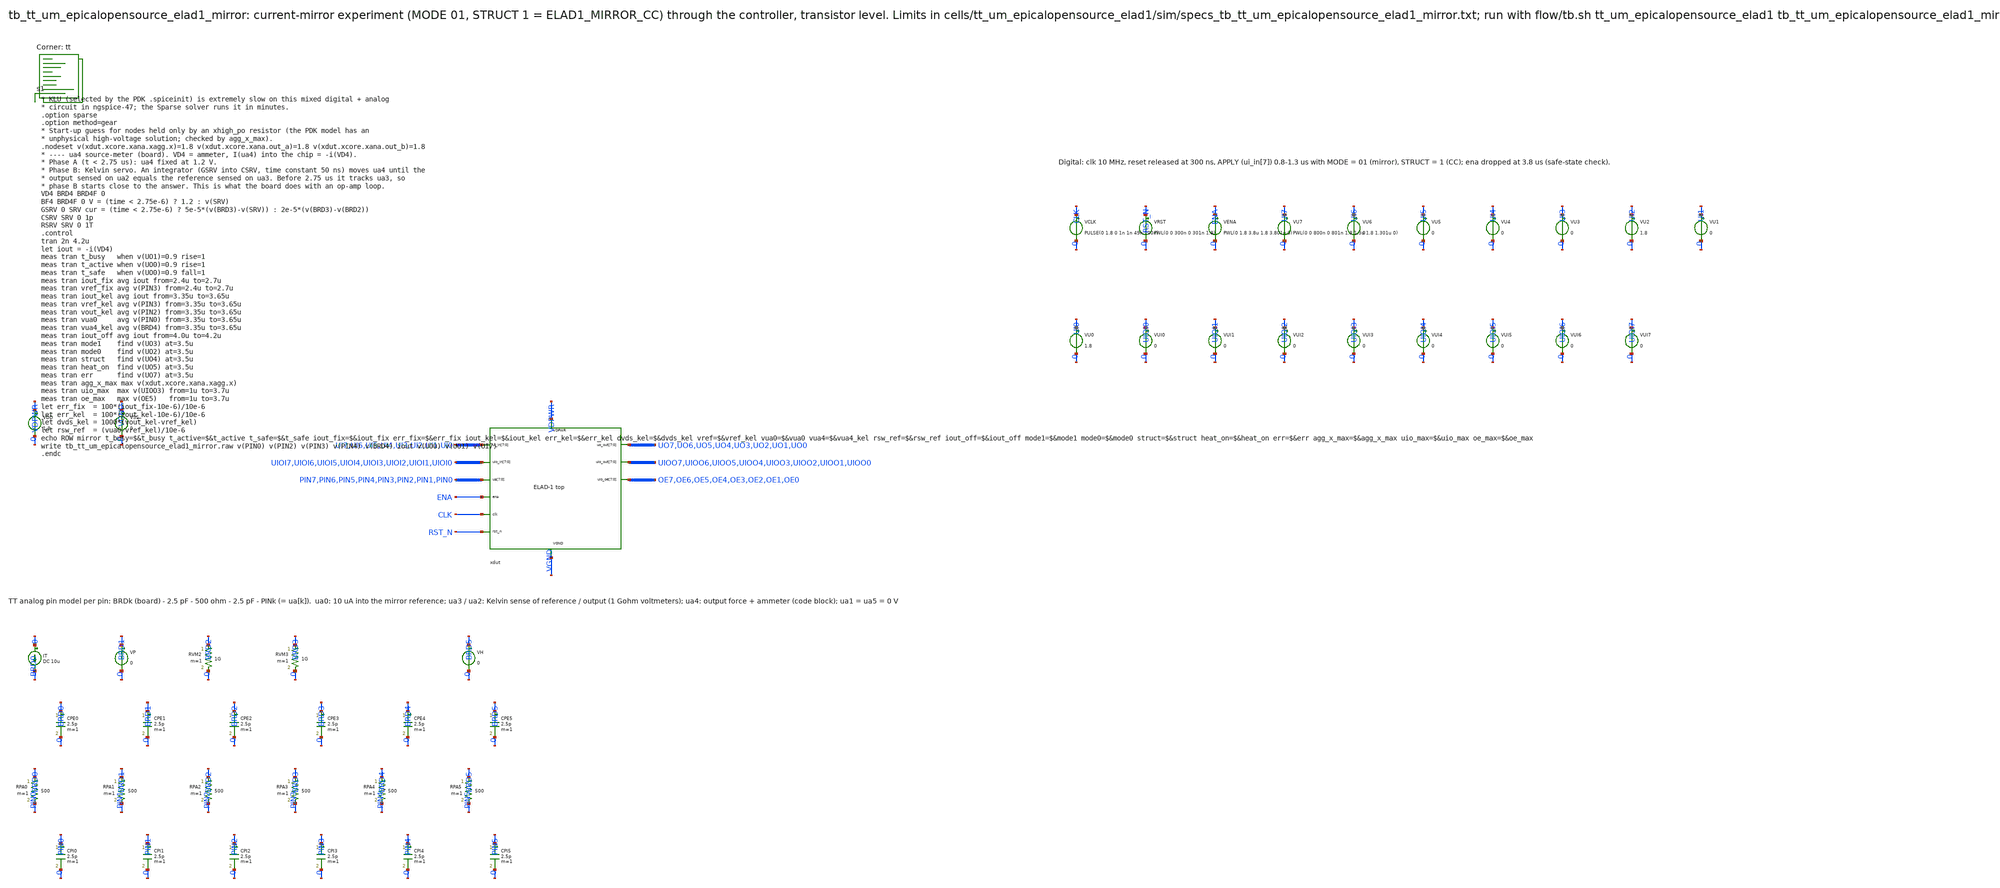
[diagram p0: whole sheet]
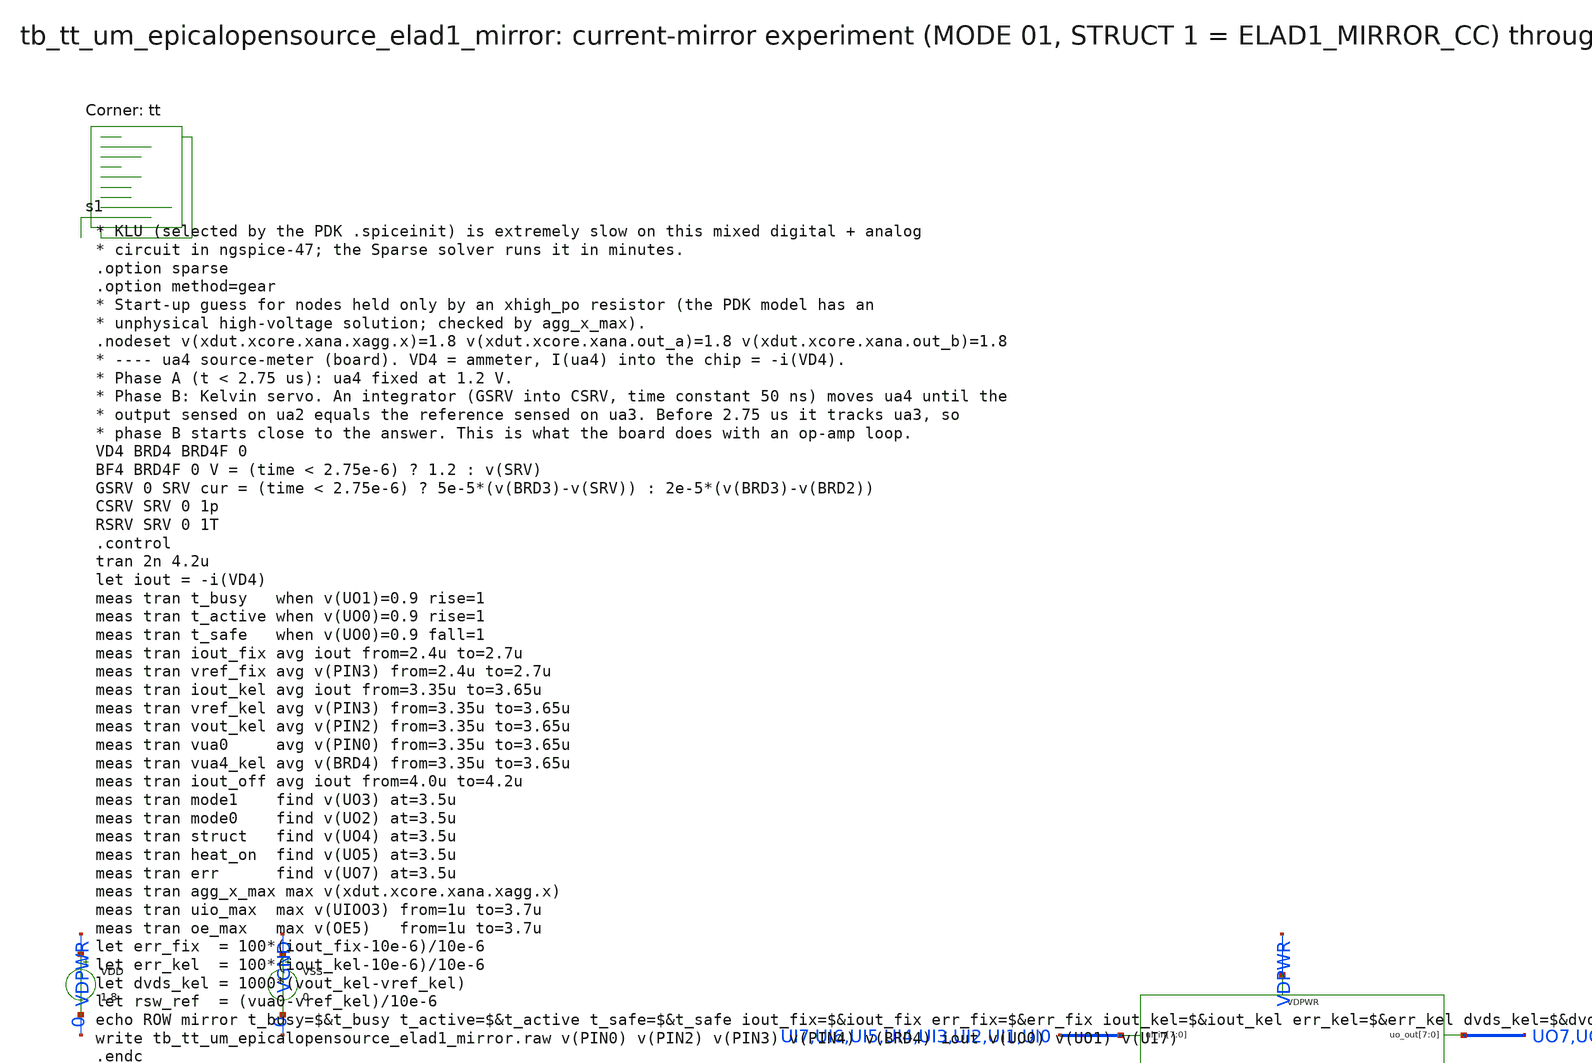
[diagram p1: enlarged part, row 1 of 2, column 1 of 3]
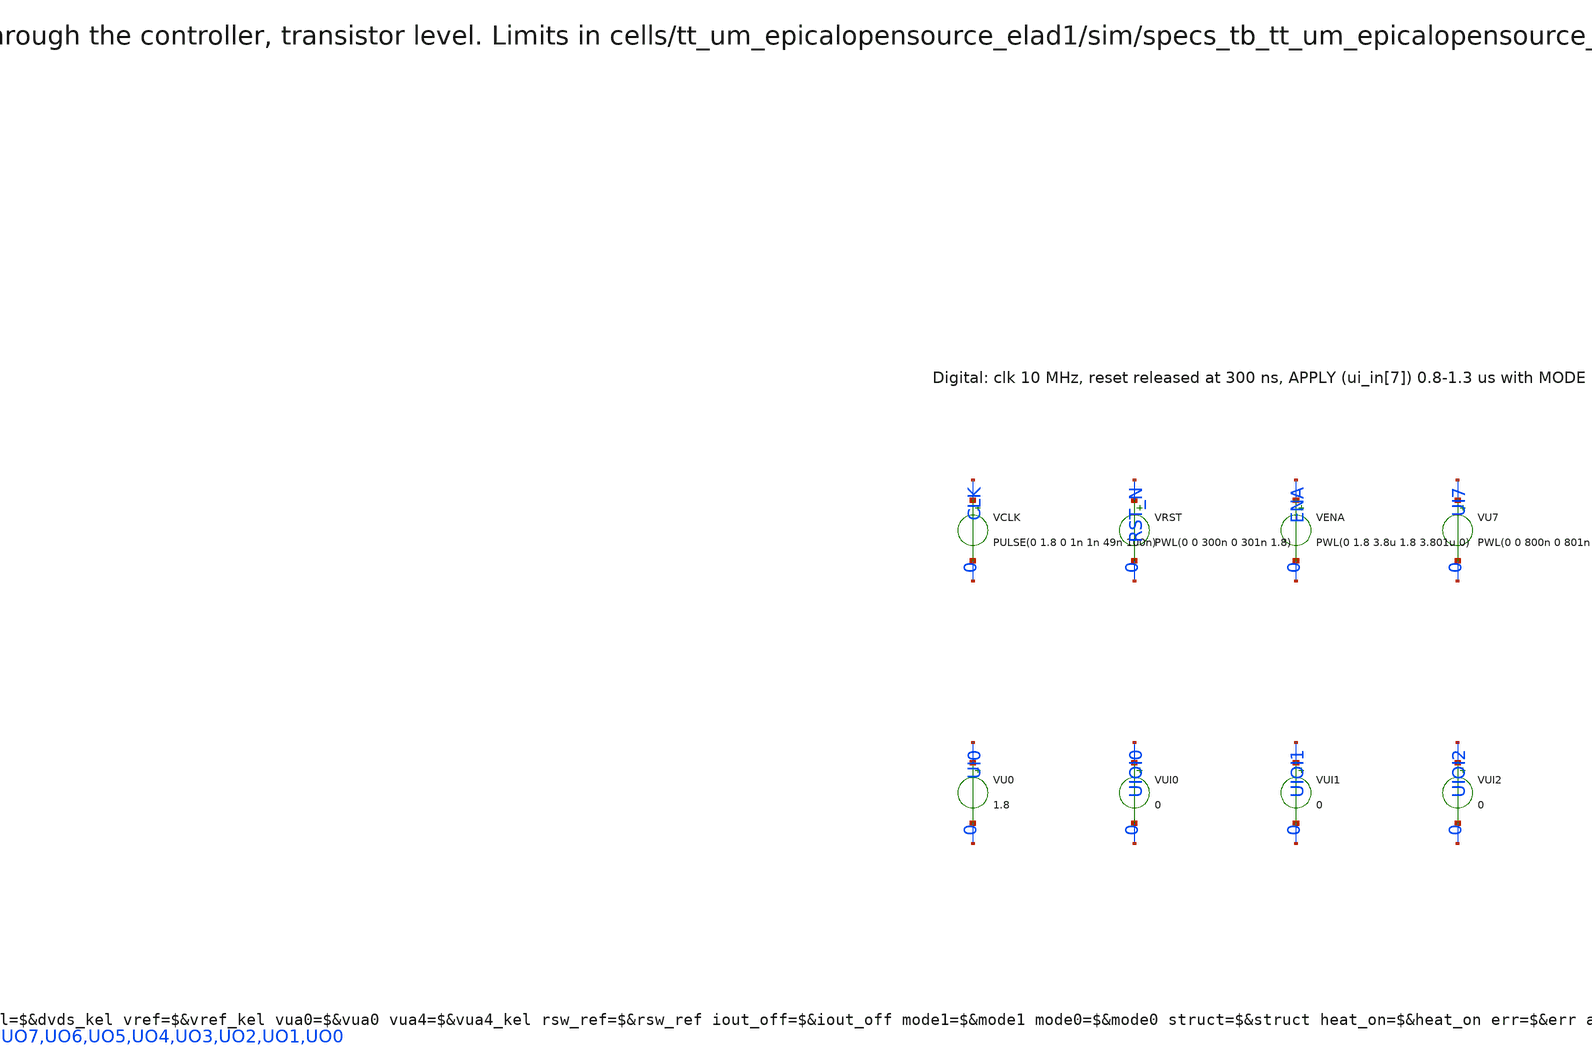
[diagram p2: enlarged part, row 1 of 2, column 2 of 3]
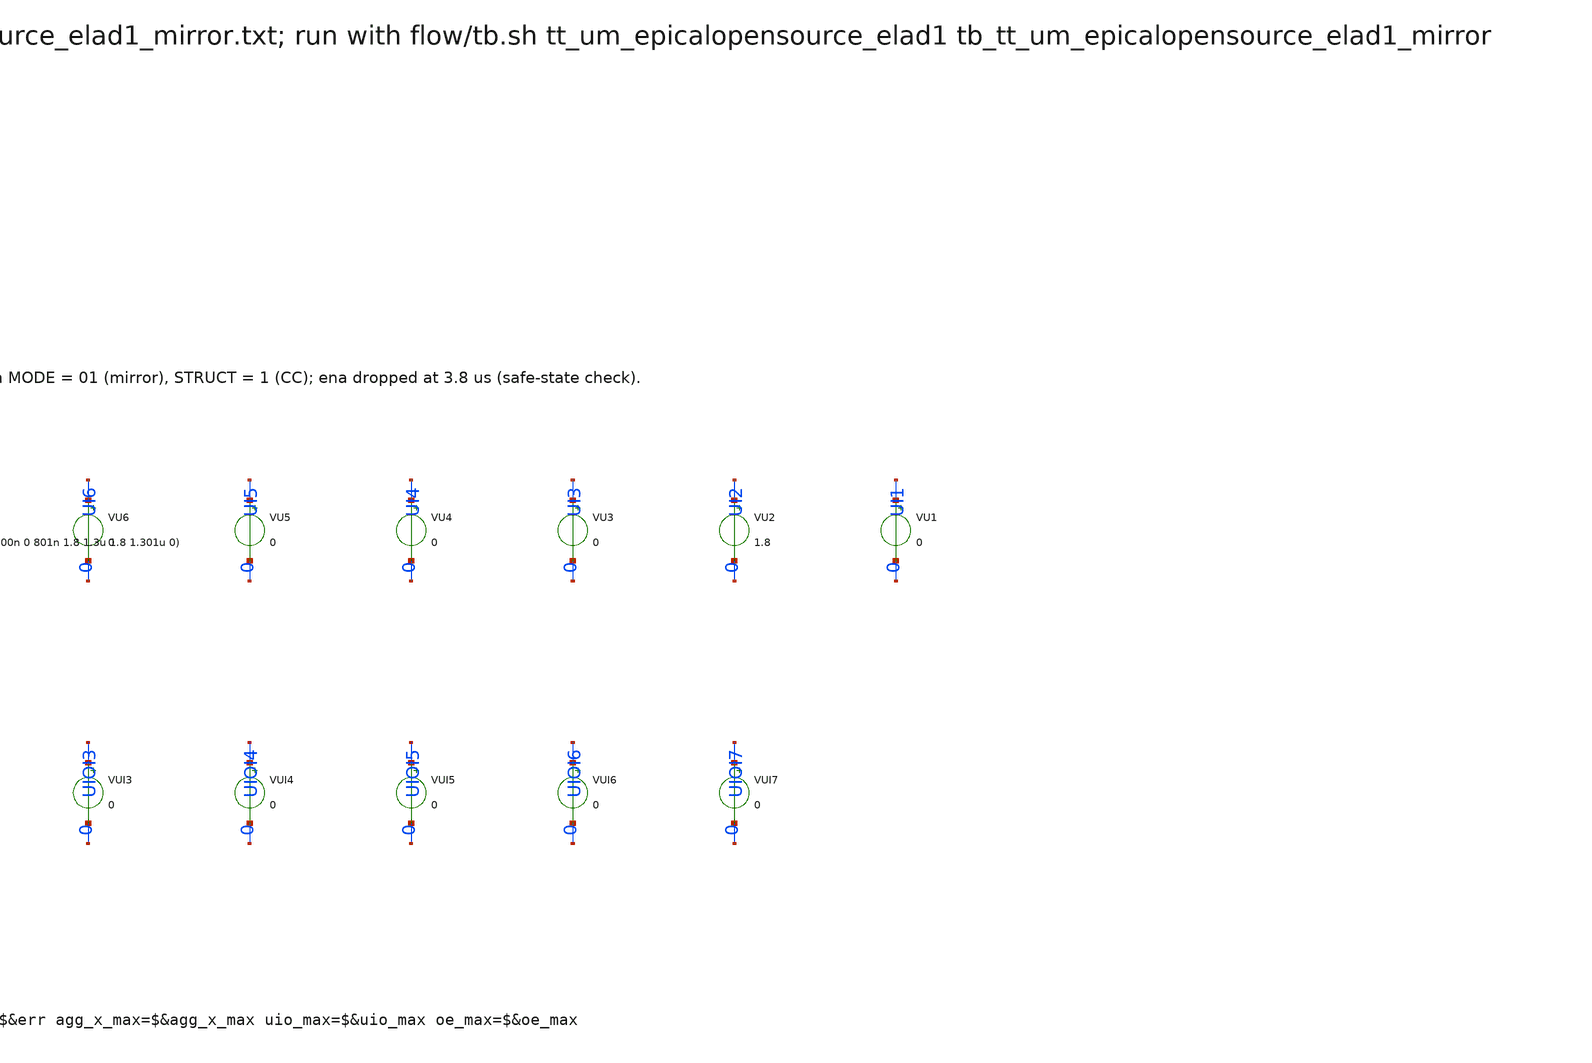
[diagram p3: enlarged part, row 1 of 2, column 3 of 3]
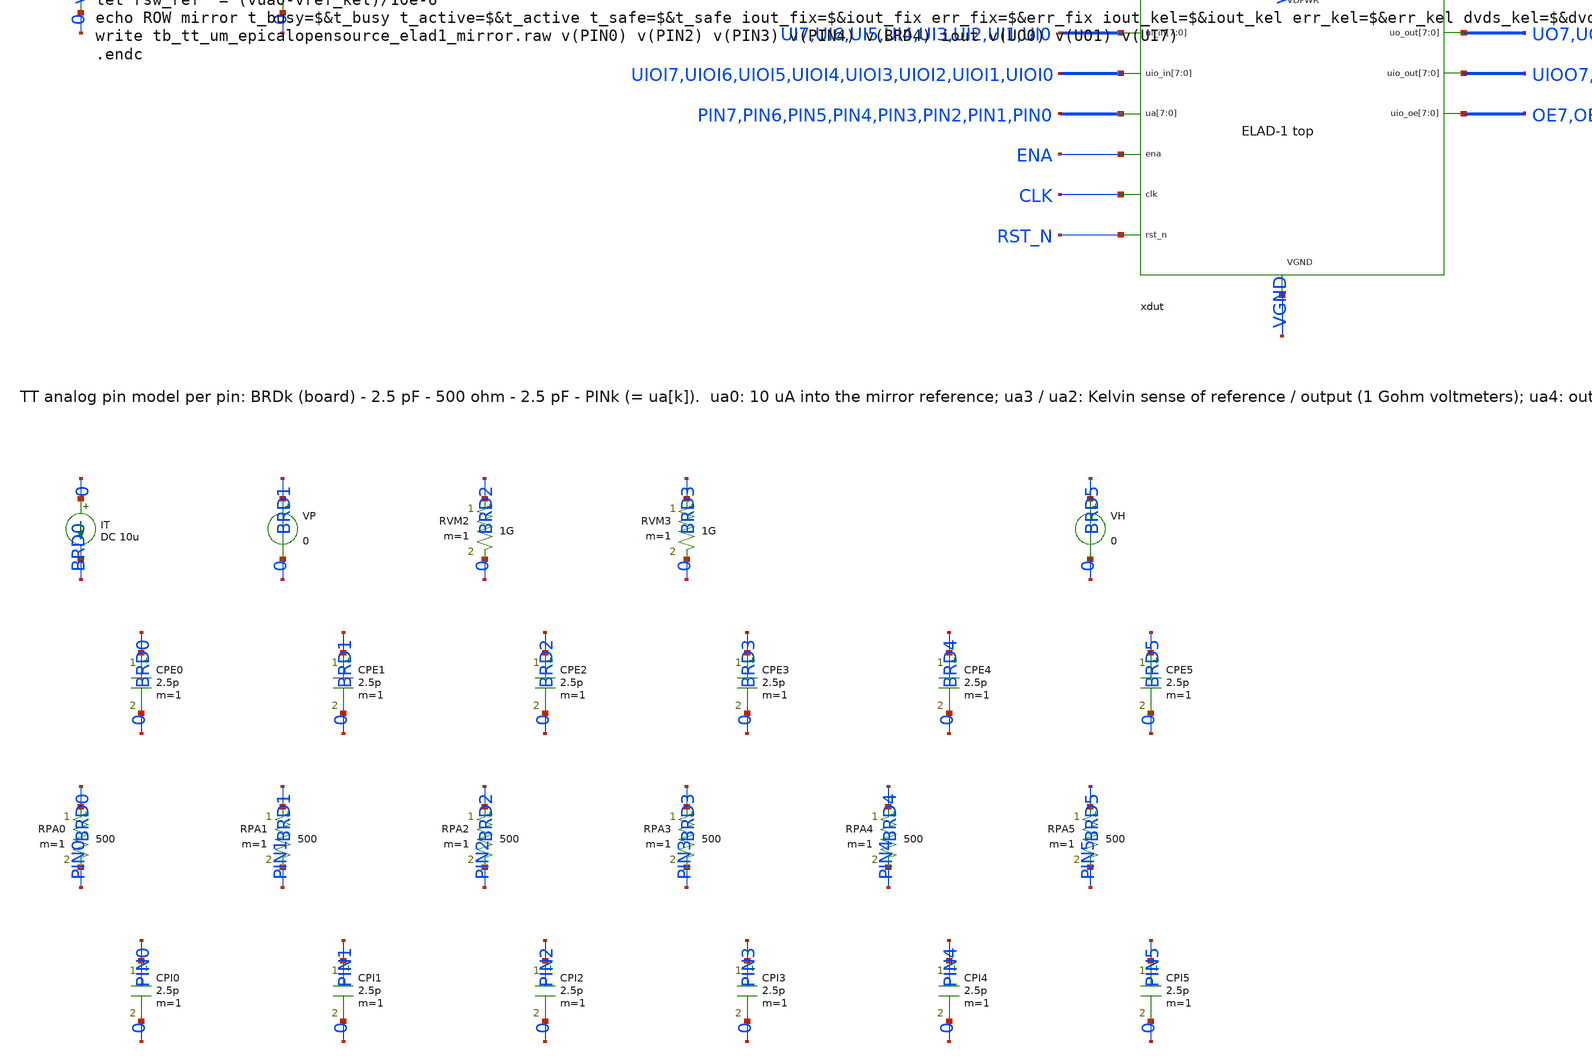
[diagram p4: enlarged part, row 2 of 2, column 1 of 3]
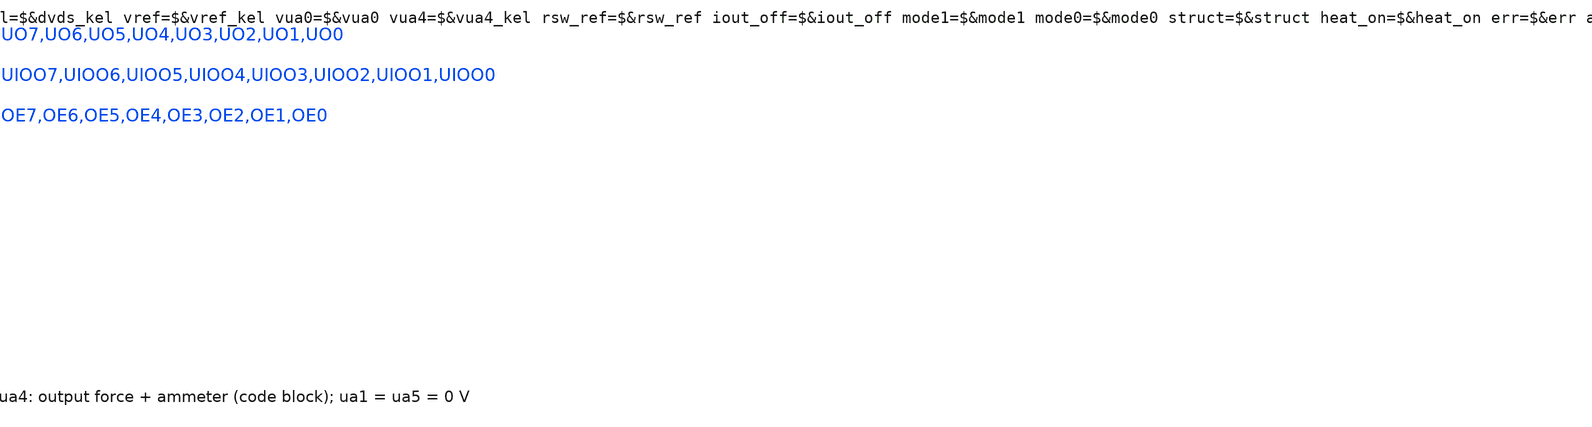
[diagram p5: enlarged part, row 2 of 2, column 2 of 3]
** sch_path: cells/tt_um_epicalopensource_elad1/schematic/tb_tt_um_epicalopensource_elad1_mirror.sch
**.subckt tb_tt_um_epicalopensource_elad1_mirror
xdut UI7 UI6 UI5 UI4 UI3 UI2 UI1 UI0 UIOI7 UIOI6 UIOI5 UIOI4 UIOI3 UIOI2 UIOI1 UIOI0 PIN7 PIN6 PIN5
+ PIN4 PIN3 PIN2 PIN1 PIN0 ENA CLK RST_N UO7 UO6 UO5 UO4 UO3 UO2 UO1 UO0 UIOO7 UIOO6 UIOO5 UIOO4 UIOO3
+ UIOO2 UIOO1 UIOO0 OE7 OE6 OE5 OE4 OE3 OE2 OE1 OE0 VDPWR VGND tt_um_epicalopensource_elad1
VDD VDPWR 0 1.8
VSS VGND 0 0
IT 0 BRD0 DC 10u
CPE0 BRD0 0 2.5p m=1
RPA0 BRD0 PIN0 500 m=1
CPI0 PIN0 0 2.5p m=1
VP BRD1 0 0
CPE1 BRD1 0 2.5p m=1
RPA1 BRD1 PIN1 500 m=1
CPI1 PIN1 0 2.5p m=1
RVM2 BRD2 0 1G m=1
CPE2 BRD2 0 2.5p m=1
RPA2 BRD2 PIN2 500 m=1
CPI2 PIN2 0 2.5p m=1
RVM3 BRD3 0 1G m=1
CPE3 BRD3 0 2.5p m=1
RPA3 BRD3 PIN3 500 m=1
CPI3 PIN3 0 2.5p m=1
CPE4 BRD4 0 2.5p m=1
RPA4 BRD4 PIN4 500 m=1
CPI4 PIN4 0 2.5p m=1
VH BRD5 0 0
CPE5 BRD5 0 2.5p m=1
RPA5 BRD5 PIN5 500 m=1
CPI5 PIN5 0 2.5p m=1
VCLK CLK 0 PULSE(0 1.8 0 1n 1n 49n 100n)
VRST RST_N 0 PWL(0 0 300n 0 301n 1.8)
VENA ENA 0 PWL(0 1.8 3.8u 1.8 3.801u 0)
VU7 UI7 0 PWL(0 0 800n 0 801n 1.8 1.3u 1.8 1.301u 0)
VU6 UI6 0 0
VU5 UI5 0 0
VU4 UI4 0 0
VU3 UI3 0 0
VU2 UI2 0 1.8
VU1 UI1 0 0
VU0 UI0 0 1.8
VUI0 UIOI0 0 0
VUI1 UIOI1 0 0
VUI2 UIOI2 0 0
VUI3 UIOI3 0 0
VUI4 UIOI4 0 0
VUI5 UIOI5 0 0
VUI6 UIOI6 0 0
VUI7 UIOI7 0 0
**** begin user architecture code
.lib $::SKYWATER_MODELS/sky130.lib.spice tt

* KLU (selected by the PDK .spiceinit) is extremely slow on this mixed digital + analog
* circuit in ngspice-47; the Sparse solver runs it in minutes.
.option sparse
.option method=gear
* Start-up guess for nodes held only by an xhigh_po resistor (the PDK model has an
* unphysical high-voltage solution; checked by agg_x_max).
.nodeset v(xdut.xcore.xana.xagg.x)=1.8 v(xdut.xcore.xana.out_a)=1.8 v(xdut.xcore.xana.out_b)=1.8
* ---- ua4 source-meter (board). VD4 = ammeter, I(ua4) into the chip = -i(VD4).
* Phase A (t < 2.75 us): ua4 fixed at 1.2 V.
* Phase B: Kelvin servo. An integrator (GSRV into CSRV, time constant 50 ns) moves ua4 until the
* output sensed on ua2 equals the reference sensed on ua3. Before 2.75 us it tracks ua3, so
* phase B starts close to the answer. This is what the board does with an op-amp loop.
VD4 BRD4 BRD4F 0
BF4 BRD4F 0 V = (time < 2.75e-6) ? 1.2 : v(SRV)
GSRV 0 SRV cur = (time < 2.75e-6) ? 5e-5*(v(BRD3)-v(SRV)) : 2e-5*(v(BRD3)-v(BRD2))
CSRV SRV 0 1p
RSRV SRV 0 1T
.control
tran 2n 4.2u
let iout = -i(VD4)
meas tran t_busy   when v(UO1)=0.9 rise=1
meas tran t_active when v(UO0)=0.9 rise=1
meas tran t_safe   when v(UO0)=0.9 fall=1
meas tran iout_fix avg iout from=2.4u to=2.7u
meas tran vref_fix avg v(PIN3) from=2.4u to=2.7u
meas tran iout_kel avg iout from=3.35u to=3.65u
meas tran vref_kel avg v(PIN3) from=3.35u to=3.65u
meas tran vout_kel avg v(PIN2) from=3.35u to=3.65u
meas tran vua0     avg v(PIN0) from=3.35u to=3.65u
meas tran vua4_kel avg v(BRD4) from=3.35u to=3.65u
meas tran iout_off avg iout from=4.0u to=4.2u
meas tran mode1    find v(UO3) at=3.5u
meas tran mode0    find v(UO2) at=3.5u
meas tran struct   find v(UO4) at=3.5u
meas tran heat_on  find v(UO5) at=3.5u
meas tran err      find v(UO7) at=3.5u
meas tran agg_x_max max v(xdut.xcore.xana.xagg.x)
meas tran uio_max  max v(UIOO3) from=1u to=3.7u
meas tran oe_max   max v(OE5)   from=1u to=3.7u
let err_fix  = 100*(iout_fix-10e-6)/10e-6
let err_kel  = 100*(iout_kel-10e-6)/10e-6
let dvds_kel = 1000*(vout_kel-vref_kel)
let rsw_ref  = (vua0-vref_kel)/10e-6
echo ROW mirror t_busy=$&t_busy t_active=$&t_active t_safe=$&t_safe iout_fix=$&iout_fix
+ err_fix=$&err_fix iout_kel=$&iout_kel err_kel=$&err_kel dvds_kel=$&dvds_kel vref=$&vref_kel vua0=$&vua0
+ vua4=$&vua4_kel rsw_ref=$&rsw_ref iout_off=$&iout_off mode1=$&mode1 mode0=$&mode0 struct=$&struct heat_on=$&heat_on
+ err=$&err agg_x_max=$&agg_x_max uio_max=$&uio_max oe_max=$&oe_max
write tb_tt_um_epicalopensource_elad1_mirror.raw v(PIN0) v(PIN2) v(PIN3) v(PIN4) v(BRD4) iout v(UO0)
+ v(UO1) v(UI7)
.endc

**** end user architecture code
**.ends
.end
